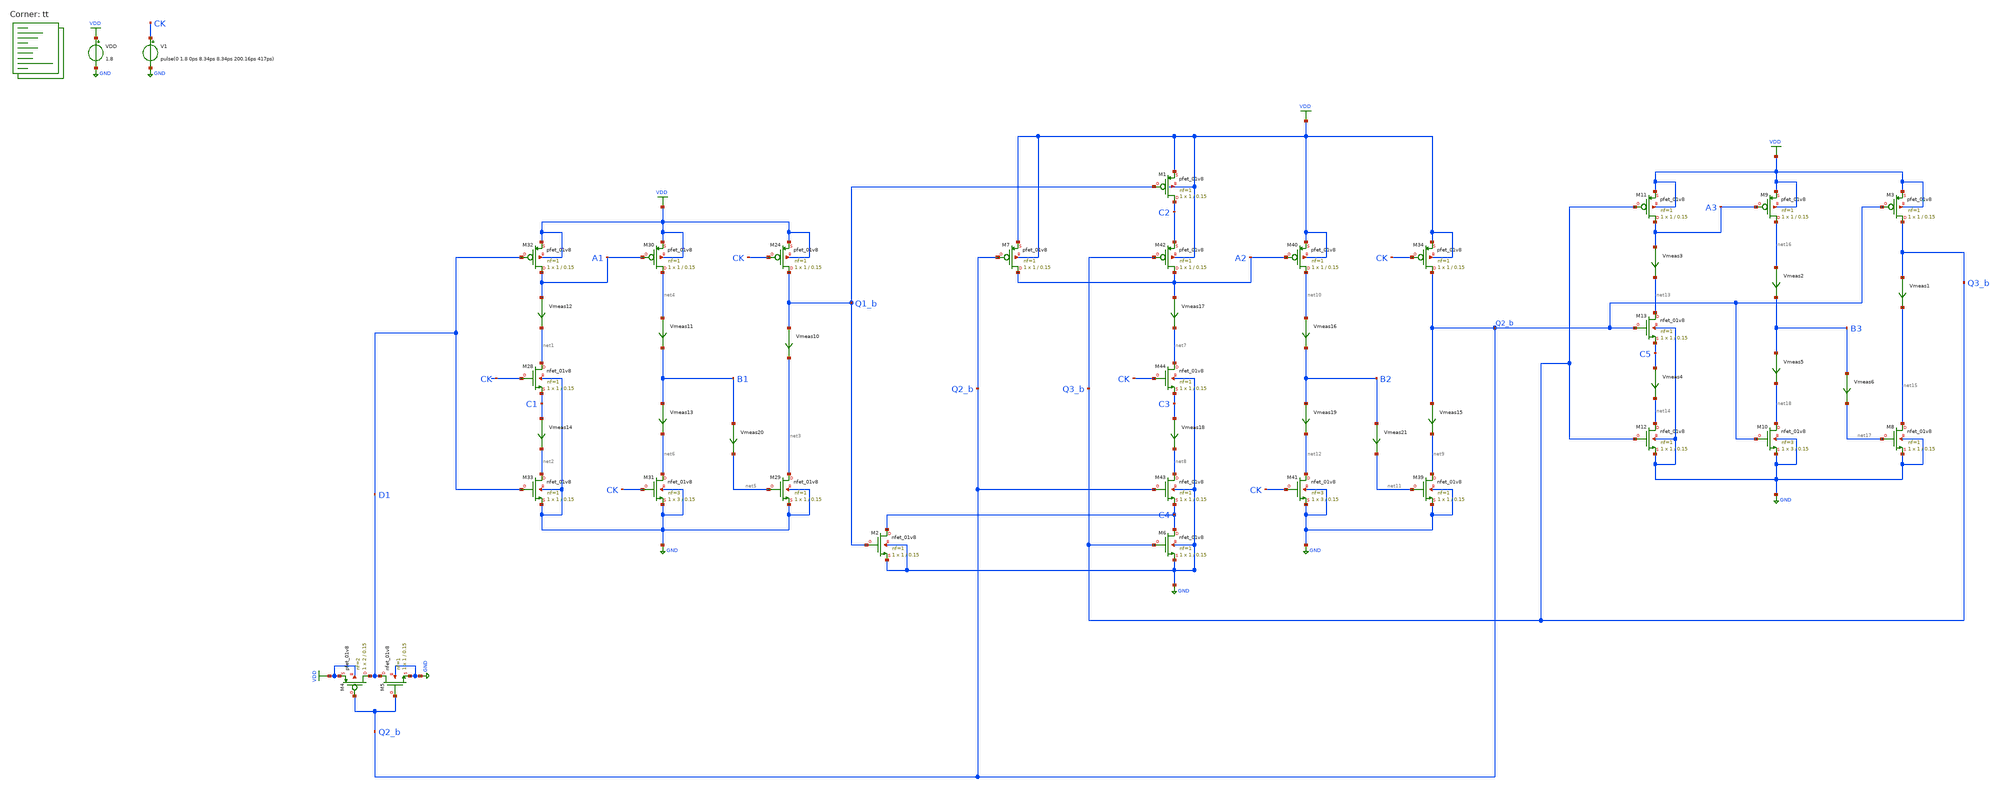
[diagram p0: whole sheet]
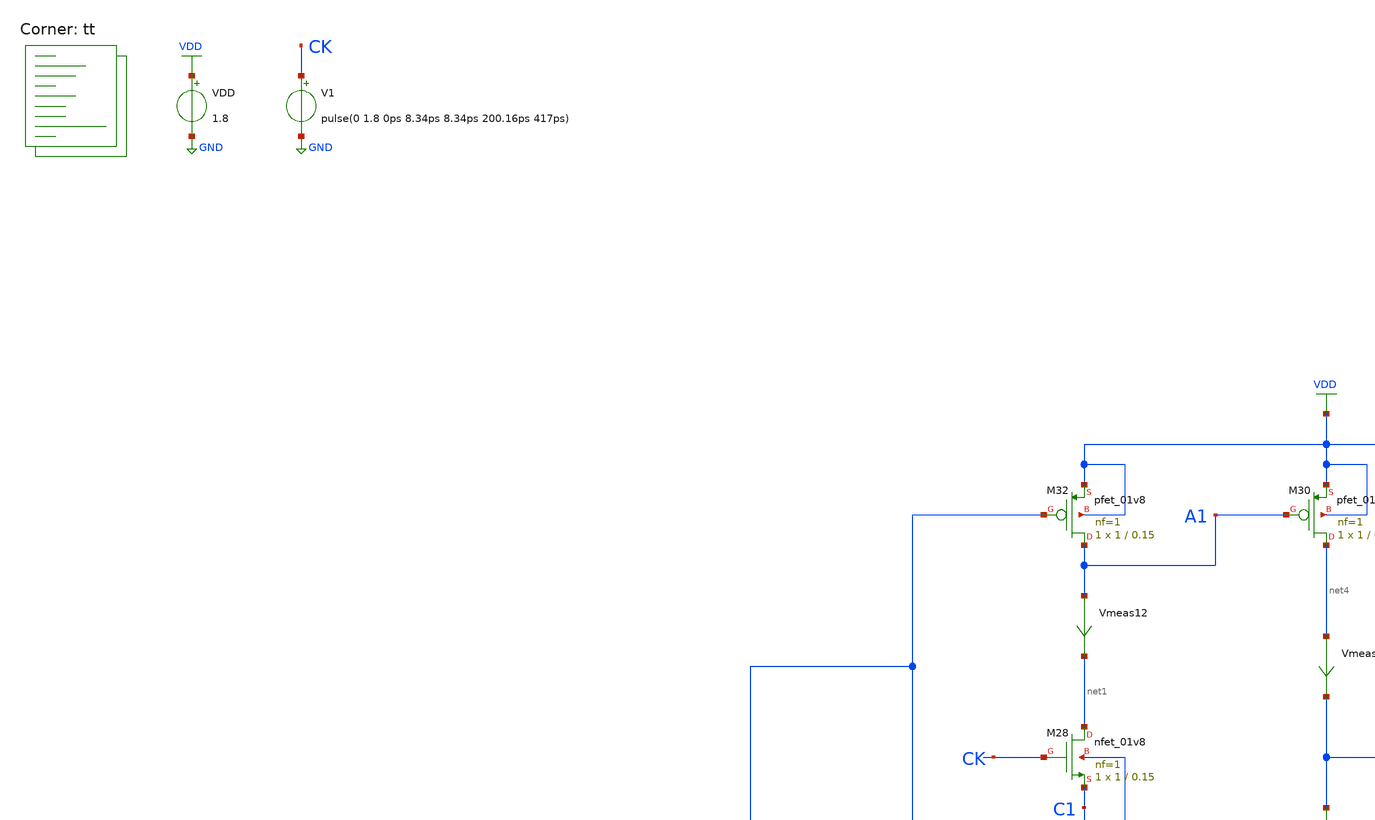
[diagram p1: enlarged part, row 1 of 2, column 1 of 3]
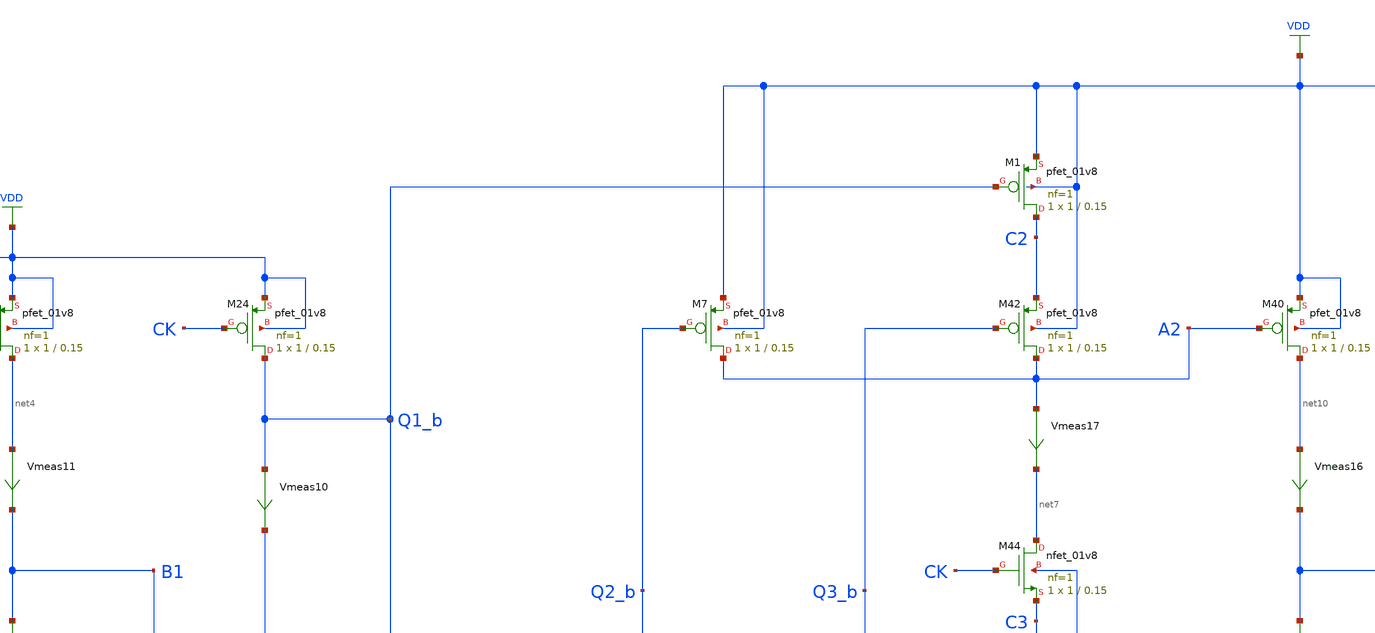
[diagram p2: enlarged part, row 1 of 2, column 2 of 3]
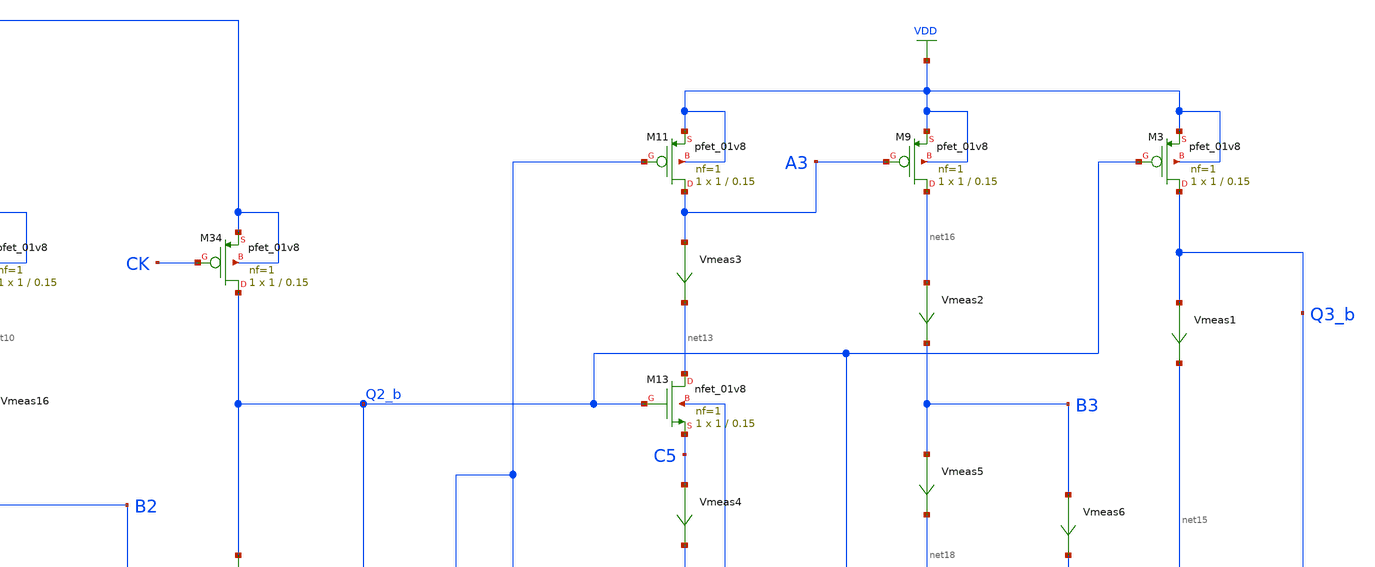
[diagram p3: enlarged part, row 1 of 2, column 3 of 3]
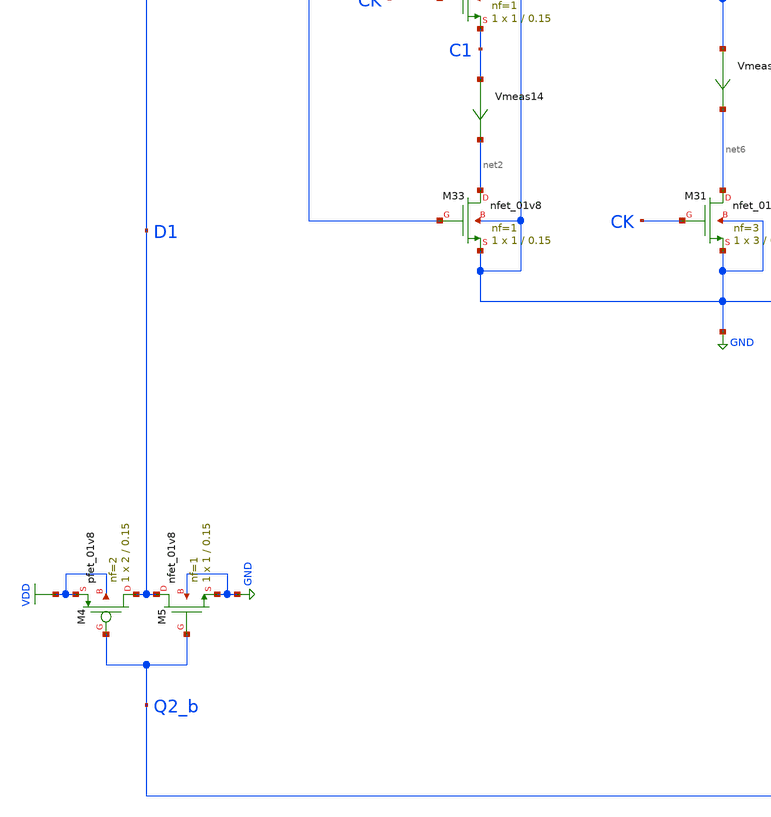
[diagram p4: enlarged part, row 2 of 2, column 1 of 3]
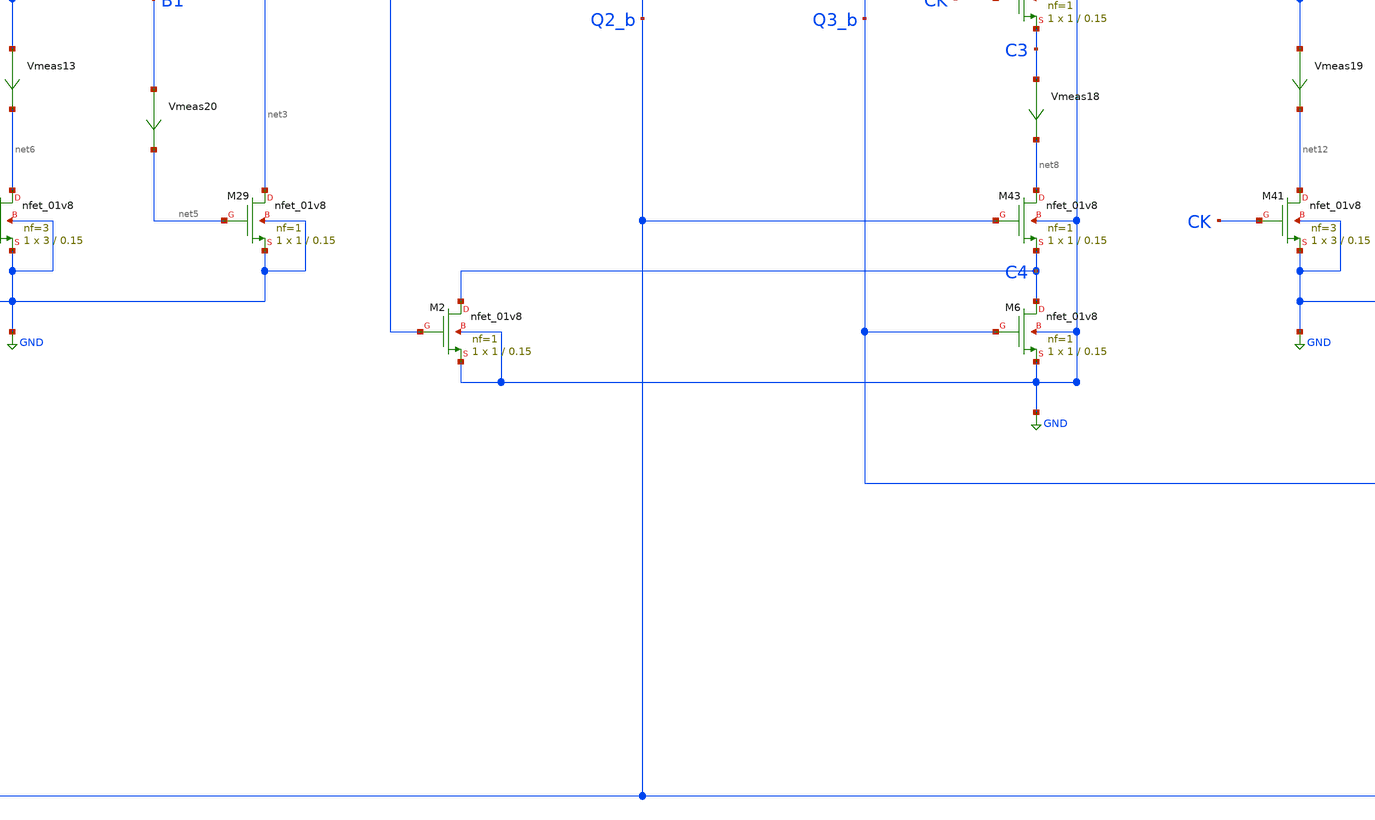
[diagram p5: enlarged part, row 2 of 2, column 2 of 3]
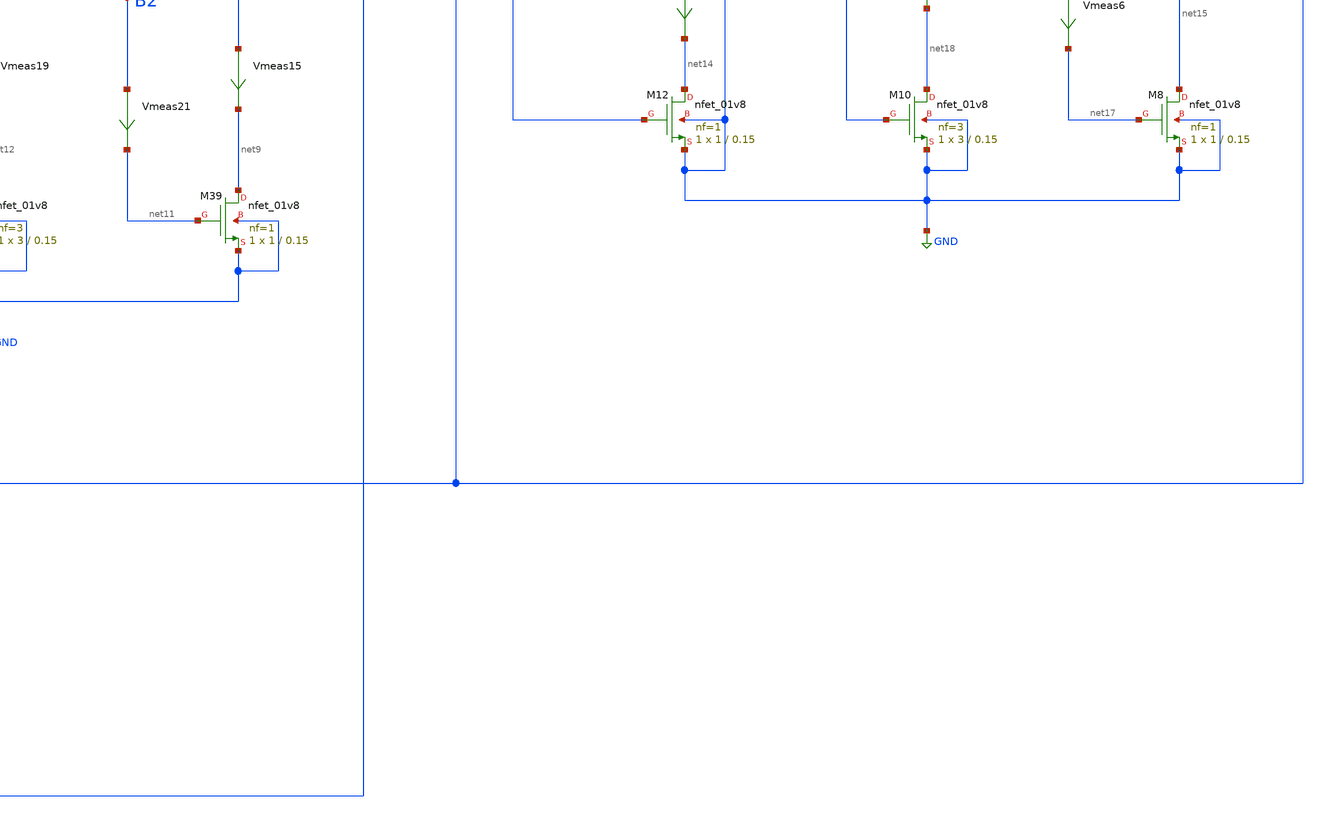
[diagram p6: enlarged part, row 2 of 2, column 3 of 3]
** sch_path: projects/pll/divider/xschem_ngspice/tb_TSPC_FF_ratioed_divide5_1.sch
**.subckt tb_TSPC_FF_ratioed_divide5_1
VDD VDD GND 1.8
XM24 Q1_b CK VDD VDD sky130_fd_pr__pfet_01v8 L=0.15 W=1 nf=1 ad='int((nf+1)/2) * W/nf * 0.29' as='int((nf+2)/2) * W/nf * 0.29'
+ pd='2*int((nf+1)/2) * (W/nf + 0.29)' ps='2*int((nf+2)/2) * (W/nf + 0.29)' nrd='0.29 / W' nrs='0.29 / W'
+ sa=0 sb=0 sd=0 mult=1 m=1
Vmeas10 Q1_b net3 0
.save i(vmeas10)
XM29 net3 net5 GND GND sky130_fd_pr__nfet_01v8 L=0.15 W=1 nf=1 ad='int((nf+1)/2) * W/nf * 0.29' as='int((nf+2)/2) * W/nf * 0.29'
+ pd='2*int((nf+1)/2) * (W/nf + 0.29)' ps='2*int((nf+2)/2) * (W/nf + 0.29)' nrd='0.29 / W' nrs='0.29 / W'
+ sa=0 sb=0 sd=0 mult=1 m=1
XM30 net4 A1 VDD VDD sky130_fd_pr__pfet_01v8 L=0.15 W=1 nf=1 ad='int((nf+1)/2) * W/nf * 0.29' as='int((nf+2)/2) * W/nf * 0.29'
+ pd='2*int((nf+1)/2) * (W/nf + 0.29)' ps='2*int((nf+2)/2) * (W/nf + 0.29)' nrd='0.29 / W' nrs='0.29 / W'
+ sa=0 sb=0 sd=0 mult=1 m=1
XM31 net6 CK GND GND sky130_fd_pr__nfet_01v8 L=0.15 W=3 nf=3 ad='int((nf+1)/2) * W/nf * 0.29' as='int((nf+2)/2) * W/nf * 0.29'
+ pd='2*int((nf+1)/2) * (W/nf + 0.29)' ps='2*int((nf+2)/2) * (W/nf + 0.29)' nrd='0.29 / W' nrs='0.29 / W'
+ sa=0 sb=0 sd=0 mult=1 m=1
Vmeas11 net4 B1 0
.save i(vmeas11)
XM32 A1 D1 VDD VDD sky130_fd_pr__pfet_01v8 L=0.15 W=1 nf=1 ad='int((nf+1)/2) * W/nf * 0.29' as='int((nf+2)/2) * W/nf * 0.29'
+ pd='2*int((nf+1)/2) * (W/nf + 0.29)' ps='2*int((nf+2)/2) * (W/nf + 0.29)' nrd='0.29 / W' nrs='0.29 / W'
+ sa=0 sb=0 sd=0 mult=1 m=1
XM33 net2 D1 GND GND sky130_fd_pr__nfet_01v8 L=0.15 W=1 nf=1 ad='int((nf+1)/2) * W/nf * 0.29' as='int((nf+2)/2) * W/nf * 0.29'
+ pd='2*int((nf+1)/2) * (W/nf + 0.29)' ps='2*int((nf+2)/2) * (W/nf + 0.29)' nrd='0.29 / W' nrs='0.29 / W'
+ sa=0 sb=0 sd=0 mult=1 m=1
Vmeas12 A1 net1 0
.save i(vmeas12)
Vmeas14 C1 net2 0
.save i(vmeas14)
XM28 net1 CK C1 GND sky130_fd_pr__nfet_01v8 L=0.15 W=1 nf=1 ad='int((nf+1)/2) * W/nf * 0.29' as='int((nf+2)/2) * W/nf * 0.29'
+ pd='2*int((nf+1)/2) * (W/nf + 0.29)' ps='2*int((nf+2)/2) * (W/nf + 0.29)' nrd='0.29 / W' nrs='0.29 / W'
+ sa=0 sb=0 sd=0 mult=1 m=1
Vmeas13 B1 net6 0
.save i(vmeas13)
Vmeas20 B1 net5 0
.save i(vmeas20)
XM34 Q2_b CK VDD VDD sky130_fd_pr__pfet_01v8 L=0.15 W=1 nf=1 ad='int((nf+1)/2) * W/nf * 0.29' as='int((nf+2)/2) * W/nf * 0.29'
+ pd='2*int((nf+1)/2) * (W/nf + 0.29)' ps='2*int((nf+2)/2) * (W/nf + 0.29)' nrd='0.29 / W' nrs='0.29 / W'
+ sa=0 sb=0 sd=0 mult=1 m=1
Vmeas15 Q2_b net9 0
.save i(vmeas15)
XM39 net9 net11 GND GND sky130_fd_pr__nfet_01v8 L=0.15 W=1 nf=1 ad='int((nf+1)/2) * W/nf * 0.29' as='int((nf+2)/2) * W/nf * 0.29'
+ pd='2*int((nf+1)/2) * (W/nf + 0.29)' ps='2*int((nf+2)/2) * (W/nf + 0.29)' nrd='0.29 / W' nrs='0.29 / W'
+ sa=0 sb=0 sd=0 mult=1 m=1
XM40 net10 A2 VDD VDD sky130_fd_pr__pfet_01v8 L=0.15 W=1 nf=1 ad='int((nf+1)/2) * W/nf * 0.29' as='int((nf+2)/2) * W/nf * 0.29'
+ pd='2*int((nf+1)/2) * (W/nf + 0.29)' ps='2*int((nf+2)/2) * (W/nf + 0.29)' nrd='0.29 / W' nrs='0.29 / W'
+ sa=0 sb=0 sd=0 mult=1 m=1
XM41 net12 CK GND GND sky130_fd_pr__nfet_01v8 L=0.15 W=3 nf=3 ad='int((nf+1)/2) * W/nf * 0.29' as='int((nf+2)/2) * W/nf * 0.29'
+ pd='2*int((nf+1)/2) * (W/nf + 0.29)' ps='2*int((nf+2)/2) * (W/nf + 0.29)' nrd='0.29 / W' nrs='0.29 / W'
+ sa=0 sb=0 sd=0 mult=1 m=1
Vmeas16 net10 B2 0
.save i(vmeas16)
XM42 A2 Q3_b C2 VDD sky130_fd_pr__pfet_01v8 L=0.15 W=1 nf=1 ad='int((nf+1)/2) * W/nf * 0.29' as='int((nf+2)/2) * W/nf * 0.29'
+ pd='2*int((nf+1)/2) * (W/nf + 0.29)' ps='2*int((nf+2)/2) * (W/nf + 0.29)' nrd='0.29 / W' nrs='0.29 / W'
+ sa=0 sb=0 sd=0 mult=1 m=1
XM43 net8 Q2_b C4 GND sky130_fd_pr__nfet_01v8 L=0.15 W=1 nf=1 ad='int((nf+1)/2) * W/nf * 0.29' as='int((nf+2)/2) * W/nf * 0.29'
+ pd='2*int((nf+1)/2) * (W/nf + 0.29)' ps='2*int((nf+2)/2) * (W/nf + 0.29)' nrd='0.29 / W' nrs='0.29 / W'
+ sa=0 sb=0 sd=0 mult=1 m=1
Vmeas17 A2 net7 0
.save i(vmeas17)
Vmeas18 C3 net8 0
.save i(vmeas18)
XM44 net7 CK C3 GND sky130_fd_pr__nfet_01v8 L=0.15 W=1 nf=1 ad='int((nf+1)/2) * W/nf * 0.29' as='int((nf+2)/2) * W/nf * 0.29'
+ pd='2*int((nf+1)/2) * (W/nf + 0.29)' ps='2*int((nf+2)/2) * (W/nf + 0.29)' nrd='0.29 / W' nrs='0.29 / W'
+ sa=0 sb=0 sd=0 mult=1 m=1
Vmeas19 B2 net12 0
.save i(vmeas19)
Vmeas21 B2 net11 0
.save i(vmeas21)
V1 CK GND pulse(0 1.8 0ps 8.34ps 8.34ps 200.16ps 417ps)
XM4 D1 Q2_b VDD VDD sky130_fd_pr__pfet_01v8 L=0.15 W=2 nf=2 ad='int((nf+1)/2) * W/nf * 0.29' as='int((nf+2)/2) * W/nf * 0.29'
+ pd='2*int((nf+1)/2) * (W/nf + 0.29)' ps='2*int((nf+2)/2) * (W/nf + 0.29)' nrd='0.29 / W' nrs='0.29 / W'
+ sa=0 sb=0 sd=0 mult=1 m=1
XM5 D1 Q2_b GND GND sky130_fd_pr__nfet_01v8 L=0.15 W=1 nf=1 ad='int((nf+1)/2) * W/nf * 0.29' as='int((nf+2)/2) * W/nf * 0.29'
+ pd='2*int((nf+1)/2) * (W/nf + 0.29)' ps='2*int((nf+2)/2) * (W/nf + 0.29)' nrd='0.29 / W' nrs='0.29 / W'
+ sa=0 sb=0 sd=0 mult=1 m=1
XM6 C4 Q3_b GND GND sky130_fd_pr__nfet_01v8 L=0.15 W=1 nf=1 ad='int((nf+1)/2) * W/nf * 0.29' as='int((nf+2)/2) * W/nf * 0.29'
+ pd='2*int((nf+1)/2) * (W/nf + 0.29)' ps='2*int((nf+2)/2) * (W/nf + 0.29)' nrd='0.29 / W' nrs='0.29 / W'
+ sa=0 sb=0 sd=0 mult=1 m=1
XM7 A2 Q2_b VDD VDD sky130_fd_pr__pfet_01v8 L=0.15 W=1 nf=1 ad='int((nf+1)/2) * W/nf * 0.29' as='int((nf+2)/2) * W/nf * 0.29'
+ pd='2*int((nf+1)/2) * (W/nf + 0.29)' ps='2*int((nf+2)/2) * (W/nf + 0.29)' nrd='0.29 / W' nrs='0.29 / W'
+ sa=0 sb=0 sd=0 mult=1 m=1
XM1 C2 Q1_b VDD VDD sky130_fd_pr__pfet_01v8 L=0.15 W=1 nf=1 ad='int((nf+1)/2) * W/nf * 0.29' as='int((nf+2)/2) * W/nf * 0.29'
+ pd='2*int((nf+1)/2) * (W/nf + 0.29)' ps='2*int((nf+2)/2) * (W/nf + 0.29)' nrd='0.29 / W' nrs='0.29 / W'
+ sa=0 sb=0 sd=0 mult=1 m=1
XM2 C4 Q1_b GND GND sky130_fd_pr__nfet_01v8 L=0.15 W=1 nf=1 ad='int((nf+1)/2) * W/nf * 0.29' as='int((nf+2)/2) * W/nf * 0.29'
+ pd='2*int((nf+1)/2) * (W/nf + 0.29)' ps='2*int((nf+2)/2) * (W/nf + 0.29)' nrd='0.29 / W' nrs='0.29 / W'
+ sa=0 sb=0 sd=0 mult=1 m=1
XM3 Q3_b Q2_b VDD VDD sky130_fd_pr__pfet_01v8 L=0.15 W=1 nf=1 ad='int((nf+1)/2) * W/nf * 0.29' as='int((nf+2)/2) * W/nf * 0.29'
+ pd='2*int((nf+1)/2) * (W/nf + 0.29)' ps='2*int((nf+2)/2) * (W/nf + 0.29)' nrd='0.29 / W' nrs='0.29 / W'
+ sa=0 sb=0 sd=0 mult=1 m=1
Vmeas1 Q3_b net15 0
.save i(vmeas1)
XM8 net15 net17 GND GND sky130_fd_pr__nfet_01v8 L=0.15 W=1 nf=1 ad='int((nf+1)/2) * W/nf * 0.29' as='int((nf+2)/2) * W/nf * 0.29'
+ pd='2*int((nf+1)/2) * (W/nf + 0.29)' ps='2*int((nf+2)/2) * (W/nf + 0.29)' nrd='0.29 / W' nrs='0.29 / W'
+ sa=0 sb=0 sd=0 mult=1 m=1
XM9 net16 A3 VDD VDD sky130_fd_pr__pfet_01v8 L=0.15 W=1 nf=1 ad='int((nf+1)/2) * W/nf * 0.29' as='int((nf+2)/2) * W/nf * 0.29'
+ pd='2*int((nf+1)/2) * (W/nf + 0.29)' ps='2*int((nf+2)/2) * (W/nf + 0.29)' nrd='0.29 / W' nrs='0.29 / W'
+ sa=0 sb=0 sd=0 mult=1 m=1
XM10 net18 Q2_b GND GND sky130_fd_pr__nfet_01v8 L=0.15 W=3 nf=3 ad='int((nf+1)/2) * W/nf * 0.29' as='int((nf+2)/2) * W/nf * 0.29'
+ pd='2*int((nf+1)/2) * (W/nf + 0.29)' ps='2*int((nf+2)/2) * (W/nf + 0.29)' nrd='0.29 / W' nrs='0.29 / W'
+ sa=0 sb=0 sd=0 mult=1 m=1
Vmeas2 net16 B3 0
.save i(vmeas2)
XM11 A3 Q3_b VDD VDD sky130_fd_pr__pfet_01v8 L=0.15 W=1 nf=1 ad='int((nf+1)/2) * W/nf * 0.29' as='int((nf+2)/2) * W/nf * 0.29'
+ pd='2*int((nf+1)/2) * (W/nf + 0.29)' ps='2*int((nf+2)/2) * (W/nf + 0.29)' nrd='0.29 / W' nrs='0.29 / W'
+ sa=0 sb=0 sd=0 mult=1 m=1
XM12 net14 Q3_b GND GND sky130_fd_pr__nfet_01v8 L=0.15 W=1 nf=1 ad='int((nf+1)/2) * W/nf * 0.29' as='int((nf+2)/2) * W/nf * 0.29'
+ pd='2*int((nf+1)/2) * (W/nf + 0.29)' ps='2*int((nf+2)/2) * (W/nf + 0.29)' nrd='0.29 / W' nrs='0.29 / W'
+ sa=0 sb=0 sd=0 mult=1 m=1
Vmeas3 A3 net13 0
.save i(vmeas3)
Vmeas4 C5 net14 0
.save i(vmeas4)
XM13 net13 Q2_b C5 GND sky130_fd_pr__nfet_01v8 L=0.15 W=1 nf=1 ad='int((nf+1)/2) * W/nf * 0.29' as='int((nf+2)/2) * W/nf * 0.29'
+ pd='2*int((nf+1)/2) * (W/nf + 0.29)' ps='2*int((nf+2)/2) * (W/nf + 0.29)' nrd='0.29 / W' nrs='0.29 / W'
+ sa=0 sb=0 sd=0 mult=1 m=1
Vmeas5 B3 net18 0
.save i(vmeas5)
Vmeas6 B3 net17 0
.save i(vmeas6)
**** begin user architecture code



.include /foss/pdks/sky130A/libs.ref/sky130_fd_sc_hd/spice/sky130_fd_sc_hd.spice

.option method=gear
.option wnflag=1
.option savecurrents


*.ic v(d)=0
*.ic v(q)=0
*.ic v(q1)=0

.control

  save v(d1) v(q1) v(q1_b) v(q2_b) v(q3_b) v(a1) v(a2) v(b1) v(b2) v(c1) v(c2) v(c3) v(c4) v(c5)
+ v(ck)
  * save all
  * tran 0.1n 1u
  tran 0.1p 20n

  remzerovec
  write tb_TSPC_FF_ratioed_divide5_1.raw
  * set appendwrite

.endc



.lib $::SKYWATER_MODELS/sky130.lib.spice tt
**** end user architecture code
**.ends
.GLOBAL GND
.GLOBAL VDD
.end
